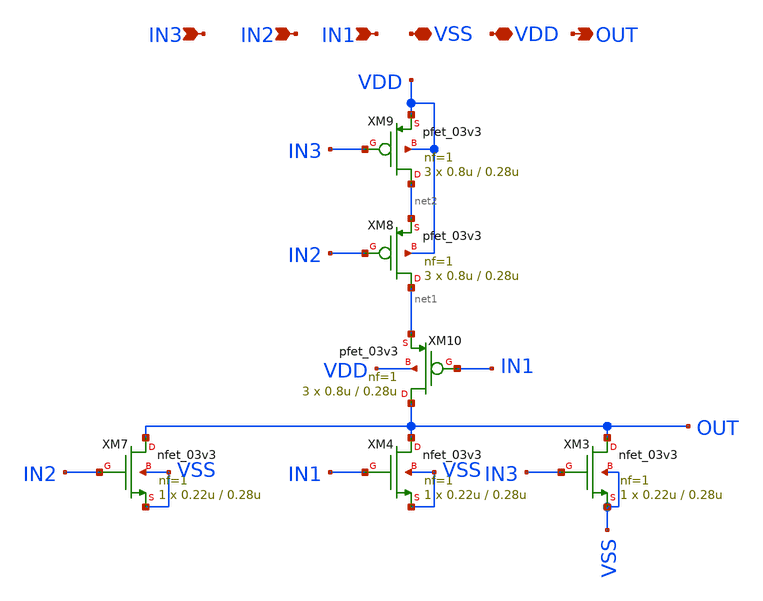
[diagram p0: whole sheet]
** sch_path: Clock_Generator_PAKISTAN_02/Schematics/nor_3.sch
**.subckt nor_3 IN2 IN1 VSS VDD OUT IN3
*.ipin IN2
*.ipin IN1
*.iopin VSS
*.iopin VDD
*.opin OUT
*.ipin IN3
XM3 OUT IN3 VSS VSS nfet_03v3 L=0.28u W=0.22u nf=1 ad='int((nf+1)/2) * W/nf * 0.18u' as='int((nf+2)/2) * W/nf * 0.18u'
+ pd='2*int((nf+1)/2) * (W/nf + 0.18u)' ps='2*int((nf+2)/2) * (W/nf + 0.18u)' nrd='0.18u / W' nrs='0.18u / W'
+ sa=0 sb=0 sd=0 m=1
XM4 OUT IN1 VSS VSS nfet_03v3 L=0.28u W=0.22u nf=1 ad='int((nf+1)/2) * W/nf * 0.18u' as='int((nf+2)/2) * W/nf * 0.18u'
+ pd='2*int((nf+1)/2) * (W/nf + 0.18u)' ps='2*int((nf+2)/2) * (W/nf + 0.18u)' nrd='0.18u / W' nrs='0.18u / W'
+ sa=0 sb=0 sd=0 m=1
XM7 OUT IN2 VSS VSS nfet_03v3 L=0.28u W=0.22u nf=1 ad='int((nf+1)/2) * W/nf * 0.18u' as='int((nf+2)/2) * W/nf * 0.18u'
+ pd='2*int((nf+1)/2) * (W/nf + 0.18u)' ps='2*int((nf+2)/2) * (W/nf + 0.18u)' nrd='0.18u / W' nrs='0.18u / W'
+ sa=0 sb=0 sd=0 m=1
XM8 net1 IN2 net2 VDD pfet_03v3 L=0.28u W=0.8u nf=1 ad='int((nf+1)/2) * W/nf * 0.18u' as='int((nf+2)/2) * W/nf * 0.18u'
+ pd='2*int((nf+1)/2) * (W/nf + 0.18u)' ps='2*int((nf+2)/2) * (W/nf + 0.18u)' nrd='0.18u / W' nrs='0.18u / W'
+ sa=0 sb=0 sd=0 m=3
XM9 net2 IN3 VDD VDD pfet_03v3 L=0.28u W=0.8u nf=1 ad='int((nf+1)/2) * W/nf * 0.18u' as='int((nf+2)/2) * W/nf * 0.18u'
+ pd='2*int((nf+1)/2) * (W/nf + 0.18u)' ps='2*int((nf+2)/2) * (W/nf + 0.18u)' nrd='0.18u / W' nrs='0.18u / W'
+ sa=0 sb=0 sd=0 m=3
XM10 OUT IN1 net1 VDD pfet_03v3 L=0.28u W=0.8u nf=1 ad='int((nf+1)/2) * W/nf * 0.18u' as='int((nf+2)/2) * W/nf * 0.18u'
+ pd='2*int((nf+1)/2) * (W/nf + 0.18u)' ps='2*int((nf+2)/2) * (W/nf + 0.18u)' nrd='0.18u / W' nrs='0.18u / W'
+ sa=0 sb=0 sd=0 m=3
**.ends
.end
